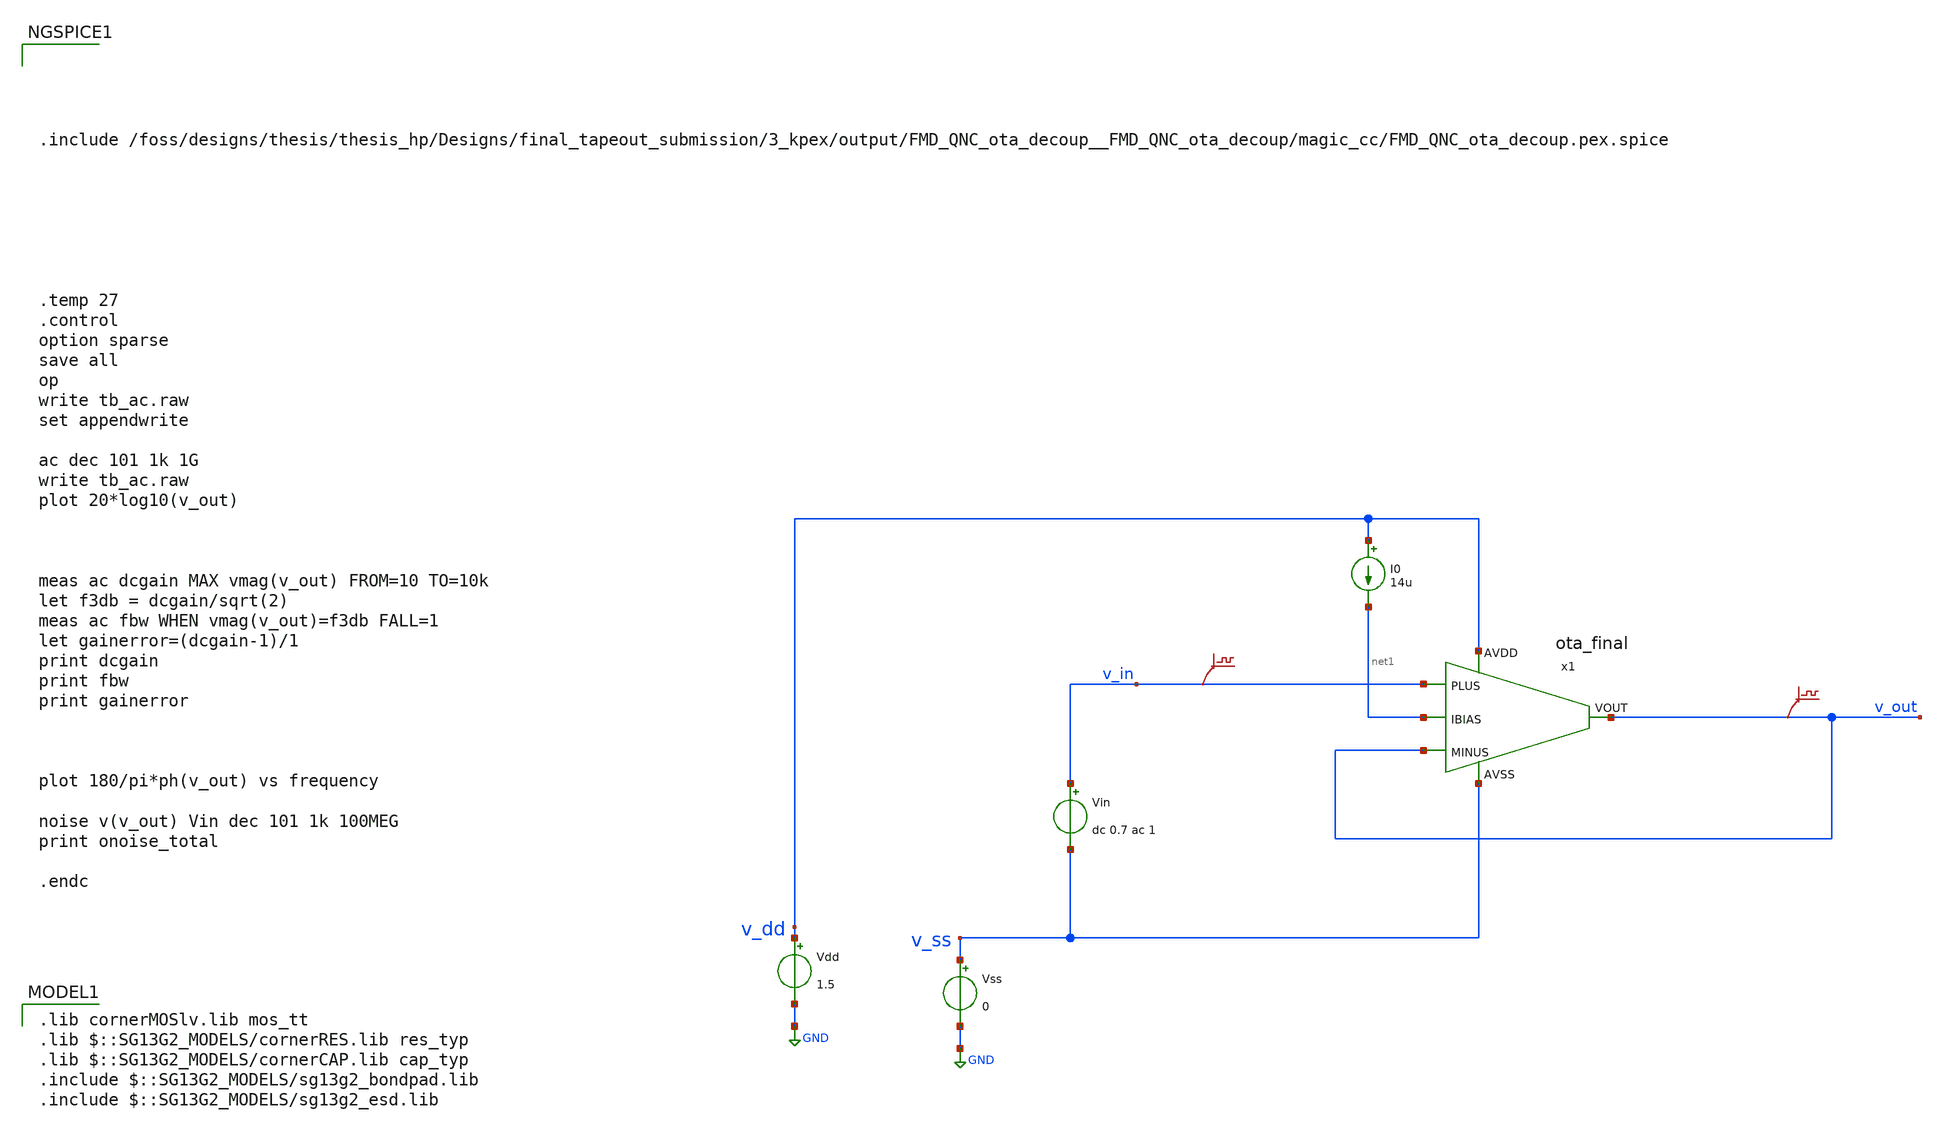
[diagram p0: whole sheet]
** sch_path: Designs/final_tapeout_submissions/OTALED/3_pex/postPEX_simulations/tb_ac.sch
* (c) 2025 Thesis_HP, Apache-2.0 license
**.subckt tb_ac
Vss v_ss GND 0
Vdd v_dd GND 1.5
Vin v_in v_ss dc 0.7 ac 1
.save v(v_in)
I0 v_dd net1 14u
.save v(v_out)
x1 v_dd net1 v_out v_out v_in v_ss ota_final
**** begin user architecture code





.include /foss/designs/thesis/thesis_hp/Designs/final_tapeout_submission/3_kpex/output/FMD_QNC_ota_decoup__FMD_QNC_ota_decoup/magic_cc/FMD_QNC_ota_decoup.pex.spice







.temp 27
.control
option sparse
save all
op
write tb_ac.raw
set appendwrite

ac dec 101 1k 1G
write tb_ac.raw
plot 20*log10(v_out)



meas ac dcgain MAX vmag(v_out) FROM=10 TO=10k
let f3db = dcgain/sqrt(2)
meas ac fbw WHEN vmag(v_out)=f3db FALL=1
let gainerror=(dcgain-1)/1
print dcgain
print fbw
print gainerror



plot 180/pi*ph(v_out) vs frequency

noise v(v_out) Vin dec 101 1k 100MEG
print onoise_total

.endc


 .lib cornerMOSlv.lib mos_tt
.lib $::SG13G2_MODELS/cornerRES.lib res_typ
.lib $::SG13G2_MODELS/cornerCAP.lib cap_typ
.include $::SG13G2_MODELS/sg13g2_bondpad.lib
.include $::SG13G2_MODELS/sg13g2_esd.lib

**** end user architecture code
**.ends
.GLOBAL GND
.end
